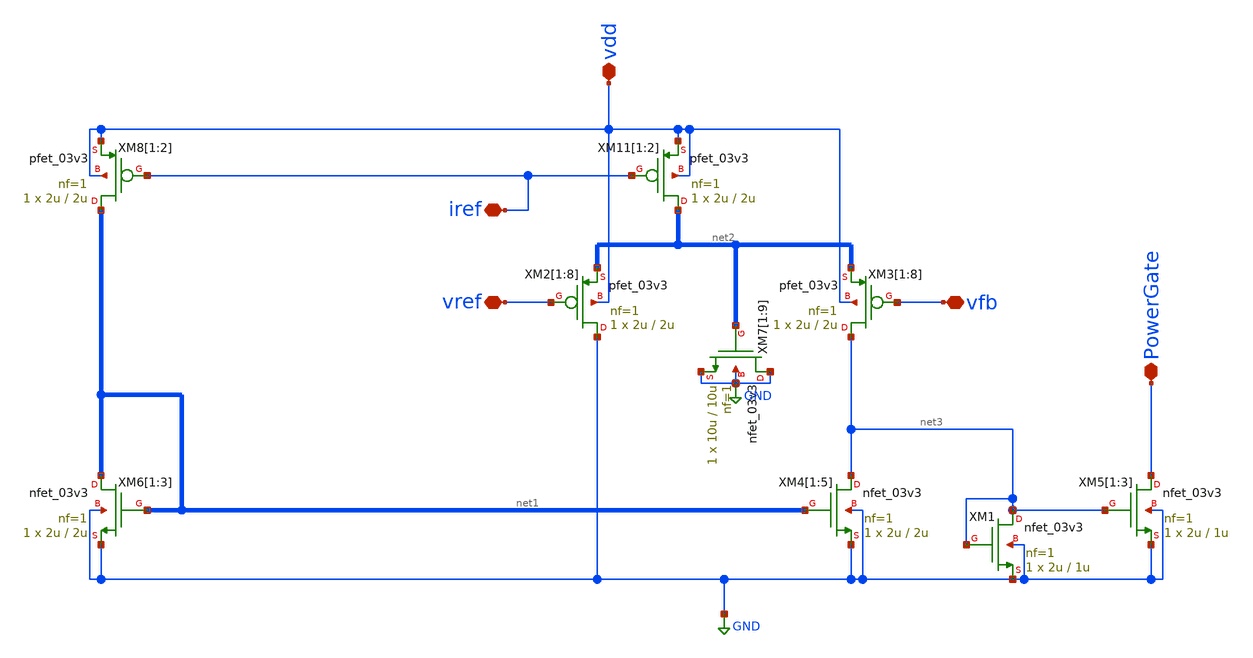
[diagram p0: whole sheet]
** sch_path: Voltage_Reference/LDO/UndervoltageProtection.sch
**.subckt UndervoltageProtection PowerGate vfb vref iref vdd
*.iopin PowerGate
*.iopin vfb
*.iopin vref
*.iopin iref
*.iopin vdd
XM2[1] GND vref net2[1] vdd pfet_03v3 L=2u W=2u nf=1 ad='int((nf+1)/2) * W/nf * 0.18u' as='int((nf+2)/2) * W/nf * 0.18u'
+ pd='2*int((nf+1)/2) * (W/nf + 0.18u)' ps='2*int((nf+2)/2) * (W/nf + 0.18u)' nrd='0.18u / W' nrs='0.18u / W'
+ sa=0 sb=0 sd=0 m=1
XM2[2] GND vref net2[0] vdd pfet_03v3 L=2u W=2u nf=1 ad='int((nf+1)/2) * W/nf * 0.18u' as='int((nf+2)/2) * W/nf * 0.18u'
+ pd='2*int((nf+1)/2) * (W/nf + 0.18u)' ps='2*int((nf+2)/2) * (W/nf + 0.18u)' nrd='0.18u / W' nrs='0.18u / W'
+ sa=0 sb=0 sd=0 m=1
XM2[3] GND vref net2[1] vdd pfet_03v3 L=2u W=2u nf=1 ad='int((nf+1)/2) * W/nf * 0.18u' as='int((nf+2)/2) * W/nf * 0.18u'
+ pd='2*int((nf+1)/2) * (W/nf + 0.18u)' ps='2*int((nf+2)/2) * (W/nf + 0.18u)' nrd='0.18u / W' nrs='0.18u / W'
+ sa=0 sb=0 sd=0 m=1
XM2[4] GND vref net2[0] vdd pfet_03v3 L=2u W=2u nf=1 ad='int((nf+1)/2) * W/nf * 0.18u' as='int((nf+2)/2) * W/nf * 0.18u'
+ pd='2*int((nf+1)/2) * (W/nf + 0.18u)' ps='2*int((nf+2)/2) * (W/nf + 0.18u)' nrd='0.18u / W' nrs='0.18u / W'
+ sa=0 sb=0 sd=0 m=1
XM2[5] GND vref net2[1] vdd pfet_03v3 L=2u W=2u nf=1 ad='int((nf+1)/2) * W/nf * 0.18u' as='int((nf+2)/2) * W/nf * 0.18u'
+ pd='2*int((nf+1)/2) * (W/nf + 0.18u)' ps='2*int((nf+2)/2) * (W/nf + 0.18u)' nrd='0.18u / W' nrs='0.18u / W'
+ sa=0 sb=0 sd=0 m=1
XM2[6] GND vref net2[0] vdd pfet_03v3 L=2u W=2u nf=1 ad='int((nf+1)/2) * W/nf * 0.18u' as='int((nf+2)/2) * W/nf * 0.18u'
+ pd='2*int((nf+1)/2) * (W/nf + 0.18u)' ps='2*int((nf+2)/2) * (W/nf + 0.18u)' nrd='0.18u / W' nrs='0.18u / W'
+ sa=0 sb=0 sd=0 m=1
XM2[7] GND vref net2[1] vdd pfet_03v3 L=2u W=2u nf=1 ad='int((nf+1)/2) * W/nf * 0.18u' as='int((nf+2)/2) * W/nf * 0.18u'
+ pd='2*int((nf+1)/2) * (W/nf + 0.18u)' ps='2*int((nf+2)/2) * (W/nf + 0.18u)' nrd='0.18u / W' nrs='0.18u / W'
+ sa=0 sb=0 sd=0 m=1
XM2[8] GND vref net2[0] vdd pfet_03v3 L=2u W=2u nf=1 ad='int((nf+1)/2) * W/nf * 0.18u' as='int((nf+2)/2) * W/nf * 0.18u'
+ pd='2*int((nf+1)/2) * (W/nf + 0.18u)' ps='2*int((nf+2)/2) * (W/nf + 0.18u)' nrd='0.18u / W' nrs='0.18u / W'
+ sa=0 sb=0 sd=0 m=1
XM3[1] net3 vfb net2[1] vdd pfet_03v3 L=2u W=2u nf=1 ad='int((nf+1)/2) * W/nf * 0.18u' as='int((nf+2)/2) * W/nf * 0.18u'
+ pd='2*int((nf+1)/2) * (W/nf + 0.18u)' ps='2*int((nf+2)/2) * (W/nf + 0.18u)' nrd='0.18u / W' nrs='0.18u / W'
+ sa=0 sb=0 sd=0 m=1
XM3[2] net3 vfb net2[0] vdd pfet_03v3 L=2u W=2u nf=1 ad='int((nf+1)/2) * W/nf * 0.18u' as='int((nf+2)/2) * W/nf * 0.18u'
+ pd='2*int((nf+1)/2) * (W/nf + 0.18u)' ps='2*int((nf+2)/2) * (W/nf + 0.18u)' nrd='0.18u / W' nrs='0.18u / W'
+ sa=0 sb=0 sd=0 m=1
XM3[3] net3 vfb net2[1] vdd pfet_03v3 L=2u W=2u nf=1 ad='int((nf+1)/2) * W/nf * 0.18u' as='int((nf+2)/2) * W/nf * 0.18u'
+ pd='2*int((nf+1)/2) * (W/nf + 0.18u)' ps='2*int((nf+2)/2) * (W/nf + 0.18u)' nrd='0.18u / W' nrs='0.18u / W'
+ sa=0 sb=0 sd=0 m=1
XM3[4] net3 vfb net2[0] vdd pfet_03v3 L=2u W=2u nf=1 ad='int((nf+1)/2) * W/nf * 0.18u' as='int((nf+2)/2) * W/nf * 0.18u'
+ pd='2*int((nf+1)/2) * (W/nf + 0.18u)' ps='2*int((nf+2)/2) * (W/nf + 0.18u)' nrd='0.18u / W' nrs='0.18u / W'
+ sa=0 sb=0 sd=0 m=1
XM3[5] net3 vfb net2[1] vdd pfet_03v3 L=2u W=2u nf=1 ad='int((nf+1)/2) * W/nf * 0.18u' as='int((nf+2)/2) * W/nf * 0.18u'
+ pd='2*int((nf+1)/2) * (W/nf + 0.18u)' ps='2*int((nf+2)/2) * (W/nf + 0.18u)' nrd='0.18u / W' nrs='0.18u / W'
+ sa=0 sb=0 sd=0 m=1
XM3[6] net3 vfb net2[0] vdd pfet_03v3 L=2u W=2u nf=1 ad='int((nf+1)/2) * W/nf * 0.18u' as='int((nf+2)/2) * W/nf * 0.18u'
+ pd='2*int((nf+1)/2) * (W/nf + 0.18u)' ps='2*int((nf+2)/2) * (W/nf + 0.18u)' nrd='0.18u / W' nrs='0.18u / W'
+ sa=0 sb=0 sd=0 m=1
XM3[7] net3 vfb net2[1] vdd pfet_03v3 L=2u W=2u nf=1 ad='int((nf+1)/2) * W/nf * 0.18u' as='int((nf+2)/2) * W/nf * 0.18u'
+ pd='2*int((nf+1)/2) * (W/nf + 0.18u)' ps='2*int((nf+2)/2) * (W/nf + 0.18u)' nrd='0.18u / W' nrs='0.18u / W'
+ sa=0 sb=0 sd=0 m=1
XM3[8] net3 vfb net2[0] vdd pfet_03v3 L=2u W=2u nf=1 ad='int((nf+1)/2) * W/nf * 0.18u' as='int((nf+2)/2) * W/nf * 0.18u'
+ pd='2*int((nf+1)/2) * (W/nf + 0.18u)' ps='2*int((nf+2)/2) * (W/nf + 0.18u)' nrd='0.18u / W' nrs='0.18u / W'
+ sa=0 sb=0 sd=0 m=1
XM4[1] net3 net1[1] GND GND nfet_03v3 L=2u W=2u nf=1 ad='int((nf+1)/2) * W/nf * 0.18u' as='int((nf+2)/2) * W/nf * 0.18u'
+ pd='2*int((nf+1)/2) * (W/nf + 0.18u)' ps='2*int((nf+2)/2) * (W/nf + 0.18u)' nrd='0.18u / W' nrs='0.18u / W'
+ sa=0 sb=0 sd=0 m=1
XM4[2] net3 net1[0] GND GND nfet_03v3 L=2u W=2u nf=1 ad='int((nf+1)/2) * W/nf * 0.18u' as='int((nf+2)/2) * W/nf * 0.18u'
+ pd='2*int((nf+1)/2) * (W/nf + 0.18u)' ps='2*int((nf+2)/2) * (W/nf + 0.18u)' nrd='0.18u / W' nrs='0.18u / W'
+ sa=0 sb=0 sd=0 m=1
XM4[3] net3 net1[1] GND GND nfet_03v3 L=2u W=2u nf=1 ad='int((nf+1)/2) * W/nf * 0.18u' as='int((nf+2)/2) * W/nf * 0.18u'
+ pd='2*int((nf+1)/2) * (W/nf + 0.18u)' ps='2*int((nf+2)/2) * (W/nf + 0.18u)' nrd='0.18u / W' nrs='0.18u / W'
+ sa=0 sb=0 sd=0 m=1
XM4[4] net3 net1[0] GND GND nfet_03v3 L=2u W=2u nf=1 ad='int((nf+1)/2) * W/nf * 0.18u' as='int((nf+2)/2) * W/nf * 0.18u'
+ pd='2*int((nf+1)/2) * (W/nf + 0.18u)' ps='2*int((nf+2)/2) * (W/nf + 0.18u)' nrd='0.18u / W' nrs='0.18u / W'
+ sa=0 sb=0 sd=0 m=1
XM4[5] net3 net1[1] GND GND nfet_03v3 L=2u W=2u nf=1 ad='int((nf+1)/2) * W/nf * 0.18u' as='int((nf+2)/2) * W/nf * 0.18u'
+ pd='2*int((nf+1)/2) * (W/nf + 0.18u)' ps='2*int((nf+2)/2) * (W/nf + 0.18u)' nrd='0.18u / W' nrs='0.18u / W'
+ sa=0 sb=0 sd=0 m=1
XM5[1] PowerGate net3 GND GND nfet_03v3 L=1u W=2u nf=1 ad='int((nf+1)/2) * W/nf * 0.18u' as='int((nf+2)/2) * W/nf * 0.18u'
+ pd='2*int((nf+1)/2) * (W/nf + 0.18u)' ps='2*int((nf+2)/2) * (W/nf + 0.18u)' nrd='0.18u / W' nrs='0.18u / W'
+ sa=0 sb=0 sd=0 m=1
XM5[2] PowerGate net3 GND GND nfet_03v3 L=1u W=2u nf=1 ad='int((nf+1)/2) * W/nf * 0.18u' as='int((nf+2)/2) * W/nf * 0.18u'
+ pd='2*int((nf+1)/2) * (W/nf + 0.18u)' ps='2*int((nf+2)/2) * (W/nf + 0.18u)' nrd='0.18u / W' nrs='0.18u / W'
+ sa=0 sb=0 sd=0 m=1
XM5[3] PowerGate net3 GND GND nfet_03v3 L=1u W=2u nf=1 ad='int((nf+1)/2) * W/nf * 0.18u' as='int((nf+2)/2) * W/nf * 0.18u'
+ pd='2*int((nf+1)/2) * (W/nf + 0.18u)' ps='2*int((nf+2)/2) * (W/nf + 0.18u)' nrd='0.18u / W' nrs='0.18u / W'
+ sa=0 sb=0 sd=0 m=1
XM6[1] net1[1] net1[1] GND GND nfet_03v3 L=2u W=2u nf=1 ad='int((nf+1)/2) * W/nf * 0.18u' as='int((nf+2)/2) * W/nf * 0.18u'
+ pd='2*int((nf+1)/2) * (W/nf + 0.18u)' ps='2*int((nf+2)/2) * (W/nf + 0.18u)' nrd='0.18u / W' nrs='0.18u / W'
+ sa=0 sb=0 sd=0 m=1
XM6[2] net1[0] net1[0] GND GND nfet_03v3 L=2u W=2u nf=1 ad='int((nf+1)/2) * W/nf * 0.18u' as='int((nf+2)/2) * W/nf * 0.18u'
+ pd='2*int((nf+1)/2) * (W/nf + 0.18u)' ps='2*int((nf+2)/2) * (W/nf + 0.18u)' nrd='0.18u / W' nrs='0.18u / W'
+ sa=0 sb=0 sd=0 m=1
XM6[3] net1[1] net1[1] GND GND nfet_03v3 L=2u W=2u nf=1 ad='int((nf+1)/2) * W/nf * 0.18u' as='int((nf+2)/2) * W/nf * 0.18u'
+ pd='2*int((nf+1)/2) * (W/nf + 0.18u)' ps='2*int((nf+2)/2) * (W/nf + 0.18u)' nrd='0.18u / W' nrs='0.18u / W'
+ sa=0 sb=0 sd=0 m=1
XM7[1] GND net2[1] GND GND nfet_03v3 L=10u W=10u nf=1 ad='int((nf+1)/2) * W/nf * 0.18u' as='int((nf+2)/2) * W/nf * 0.18u'
+ pd='2*int((nf+1)/2) * (W/nf + 0.18u)' ps='2*int((nf+2)/2) * (W/nf + 0.18u)' nrd='0.18u / W' nrs='0.18u / W'
+ sa=0 sb=0 sd=0 m=1
XM7[2] GND net2[0] GND GND nfet_03v3 L=10u W=10u nf=1 ad='int((nf+1)/2) * W/nf * 0.18u' as='int((nf+2)/2) * W/nf * 0.18u'
+ pd='2*int((nf+1)/2) * (W/nf + 0.18u)' ps='2*int((nf+2)/2) * (W/nf + 0.18u)' nrd='0.18u / W' nrs='0.18u / W'
+ sa=0 sb=0 sd=0 m=1
XM7[3] GND net2[1] GND GND nfet_03v3 L=10u W=10u nf=1 ad='int((nf+1)/2) * W/nf * 0.18u' as='int((nf+2)/2) * W/nf * 0.18u'
+ pd='2*int((nf+1)/2) * (W/nf + 0.18u)' ps='2*int((nf+2)/2) * (W/nf + 0.18u)' nrd='0.18u / W' nrs='0.18u / W'
+ sa=0 sb=0 sd=0 m=1
XM7[4] GND net2[0] GND GND nfet_03v3 L=10u W=10u nf=1 ad='int((nf+1)/2) * W/nf * 0.18u' as='int((nf+2)/2) * W/nf * 0.18u'
+ pd='2*int((nf+1)/2) * (W/nf + 0.18u)' ps='2*int((nf+2)/2) * (W/nf + 0.18u)' nrd='0.18u / W' nrs='0.18u / W'
+ sa=0 sb=0 sd=0 m=1
XM7[5] GND net2[1] GND GND nfet_03v3 L=10u W=10u nf=1 ad='int((nf+1)/2) * W/nf * 0.18u' as='int((nf+2)/2) * W/nf * 0.18u'
+ pd='2*int((nf+1)/2) * (W/nf + 0.18u)' ps='2*int((nf+2)/2) * (W/nf + 0.18u)' nrd='0.18u / W' nrs='0.18u / W'
+ sa=0 sb=0 sd=0 m=1
XM7[6] GND net2[0] GND GND nfet_03v3 L=10u W=10u nf=1 ad='int((nf+1)/2) * W/nf * 0.18u' as='int((nf+2)/2) * W/nf * 0.18u'
+ pd='2*int((nf+1)/2) * (W/nf + 0.18u)' ps='2*int((nf+2)/2) * (W/nf + 0.18u)' nrd='0.18u / W' nrs='0.18u / W'
+ sa=0 sb=0 sd=0 m=1
XM7[7] GND net2[1] GND GND nfet_03v3 L=10u W=10u nf=1 ad='int((nf+1)/2) * W/nf * 0.18u' as='int((nf+2)/2) * W/nf * 0.18u'
+ pd='2*int((nf+1)/2) * (W/nf + 0.18u)' ps='2*int((nf+2)/2) * (W/nf + 0.18u)' nrd='0.18u / W' nrs='0.18u / W'
+ sa=0 sb=0 sd=0 m=1
XM7[8] GND net2[0] GND GND nfet_03v3 L=10u W=10u nf=1 ad='int((nf+1)/2) * W/nf * 0.18u' as='int((nf+2)/2) * W/nf * 0.18u'
+ pd='2*int((nf+1)/2) * (W/nf + 0.18u)' ps='2*int((nf+2)/2) * (W/nf + 0.18u)' nrd='0.18u / W' nrs='0.18u / W'
+ sa=0 sb=0 sd=0 m=1
XM7[9] GND net2[1] GND GND nfet_03v3 L=10u W=10u nf=1 ad='int((nf+1)/2) * W/nf * 0.18u' as='int((nf+2)/2) * W/nf * 0.18u'
+ pd='2*int((nf+1)/2) * (W/nf + 0.18u)' ps='2*int((nf+2)/2) * (W/nf + 0.18u)' nrd='0.18u / W' nrs='0.18u / W'
+ sa=0 sb=0 sd=0 m=1
XM11[1] net2[1] iref vdd vdd pfet_03v3 L=2u W=2u nf=1 ad='int((nf+1)/2) * W/nf * 0.18u' as='int((nf+2)/2) * W/nf * 0.18u'
+ pd='2*int((nf+1)/2) * (W/nf + 0.18u)' ps='2*int((nf+2)/2) * (W/nf + 0.18u)' nrd='0.18u / W' nrs='0.18u / W'
+ sa=0 sb=0 sd=0 m=1
XM11[2] net2[0] iref vdd vdd pfet_03v3 L=2u W=2u nf=1 ad='int((nf+1)/2) * W/nf * 0.18u' as='int((nf+2)/2) * W/nf * 0.18u'
+ pd='2*int((nf+1)/2) * (W/nf + 0.18u)' ps='2*int((nf+2)/2) * (W/nf + 0.18u)' nrd='0.18u / W' nrs='0.18u / W'
+ sa=0 sb=0 sd=0 m=1
XM8[1] net1[1] iref vdd vdd pfet_03v3 L=2u W=2u nf=1 ad='int((nf+1)/2) * W/nf * 0.18u' as='int((nf+2)/2) * W/nf * 0.18u'
+ pd='2*int((nf+1)/2) * (W/nf + 0.18u)' ps='2*int((nf+2)/2) * (W/nf + 0.18u)' nrd='0.18u / W' nrs='0.18u / W'
+ sa=0 sb=0 sd=0 m=1
XM8[2] net1[0] iref vdd vdd pfet_03v3 L=2u W=2u nf=1 ad='int((nf+1)/2) * W/nf * 0.18u' as='int((nf+2)/2) * W/nf * 0.18u'
+ pd='2*int((nf+1)/2) * (W/nf + 0.18u)' ps='2*int((nf+2)/2) * (W/nf + 0.18u)' nrd='0.18u / W' nrs='0.18u / W'
+ sa=0 sb=0 sd=0 m=1
XM1 net3 net3 GND GND nfet_03v3 L=1u W=2u nf=1 ad='int((nf+1)/2) * W/nf * 0.18u' as='int((nf+2)/2) * W/nf * 0.18u'
+ pd='2*int((nf+1)/2) * (W/nf + 0.18u)' ps='2*int((nf+2)/2) * (W/nf + 0.18u)' nrd='0.18u / W' nrs='0.18u / W'
+ sa=0 sb=0 sd=0 m=1
**.ends
.GLOBAL GND
.end
